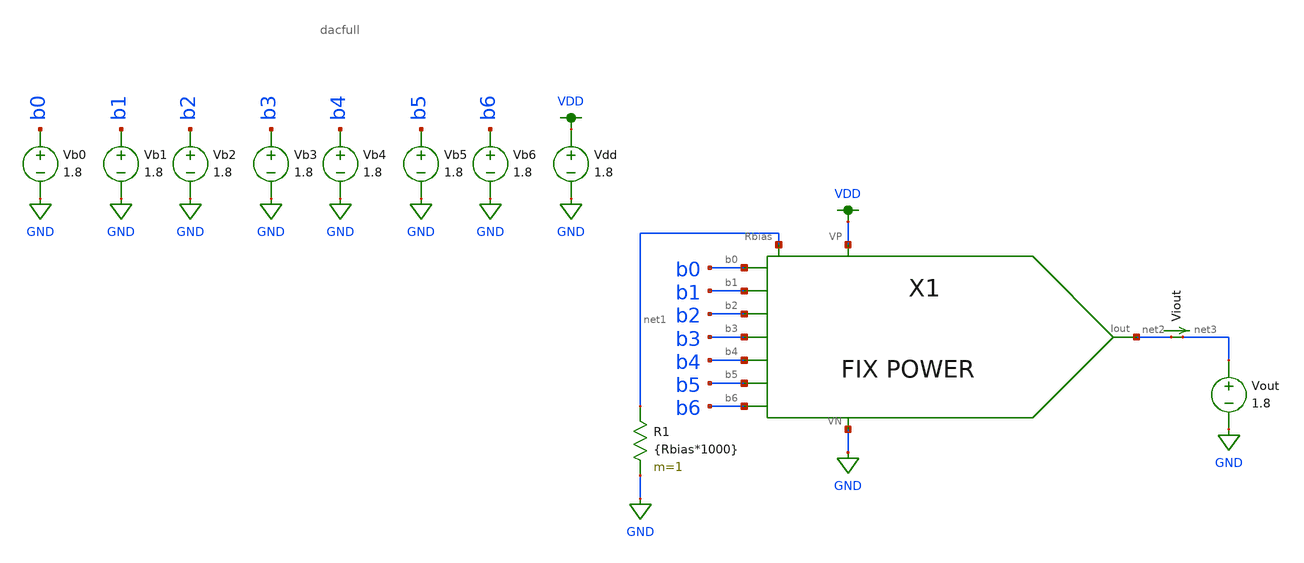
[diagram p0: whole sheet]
** sch_path: design-files/opt/dac_harness_MC_opt.sch
**.subckt dac_harness_MC_opt
X1 VDD b0 b1 b2 b3 b4 b5 b6 GND net2 net1 dacfull
Vb0 b0 GND 1.8
Vb1 b1 GND 1.8
Vb2 b2 GND 1.8
Vb3 b3 GND 1.8
Vb4 b4 GND 1.8
Vb5 b5 GND 1.8
Vb6 b6 GND 1.8
Vdd VDD GND 1.8
R1 net1 GND {Rbias*1000} m=1
Viout net2 net3 0
.save i(viout)
Vout net3 GND 1.8
**** begin user architecture code


.param llen=1.4
.param lwid=5.7
.param blen=0.5
.param bwid=1.4
.param brlen=0.3
.param brwid=3.15
.param Rbias=250
.control

	let mc_runs = 5
	let run = 1
	dowhile run <= mc_runs
		set wr_vecnames
		set wr_singlescale
		set appendwrite = FALSE
		let code = 0
		while code < 128
			if code eq 0
				let nb0 = 0
			else
				let nb0 = (code % 2)*1.8
			end
			if floor(code / 2) eq 0
				let nb1 = 0
			else
				let nb1 = (floor(code / 2) % 2)*1.8
			end
			if floor(code / 4) eq 0
				let nb2 = 0
			else
				let nb2 = (floor(code / 4) % 2)*1.8
			end
			if floor(code / 8) eq 0
				let nb3 = 0
			else
				let nb3 = (floor(code / 8) % 2)*1.8
			end
			if floor(code / 16) eq 0
				let nb4 = 0
			else
				let nb4 = (floor(code / 16) % 2)*1.8
			end
			if floor(code / 32) eq 0
				let nb5 = 0
			else
				let nb5 = (floor(code / 32) % 2)*1.8
			end
			if floor(code / 64) eq 0
				let nb6 = 0
			else
				let nb6 = (floor(code / 64) % 2)*1.8
			end
			alter Vb0 $&nb0
			alter Vb1 $&nb1
			alter Vb2 $&nb2
			alter Vb3 $&nb3
			alter Vb4 $&nb4
			alter Vb5 $&nb5
			alter Vb6 $&nb6
			save i(Viout) v(b0) v(b1) v(b2) v(b3) v(b4) v(b5) v(b6)
			op
			wrdata ~/VLSI/VLSI-MP4/design-files/opt/dacdataMC{$&run}.txt i(Viout)
			if code eq 0
				set appendwrite
				set wr_vecnames = FALSE
			end
			let code = code + 1

		end
	reset
	let run = run + 1
	end
	quit
.endc


.option wnflag=1
.param MC_SWITCH=0
.lib ~/skywater/skywater-pdk/libraries/sky130_fd_pr_ngspice/latest/models/sky130.lib.spice tt

**** end user architecture code
**.ends
.GLOBAL GND
.GLOBAL VDD
.end
